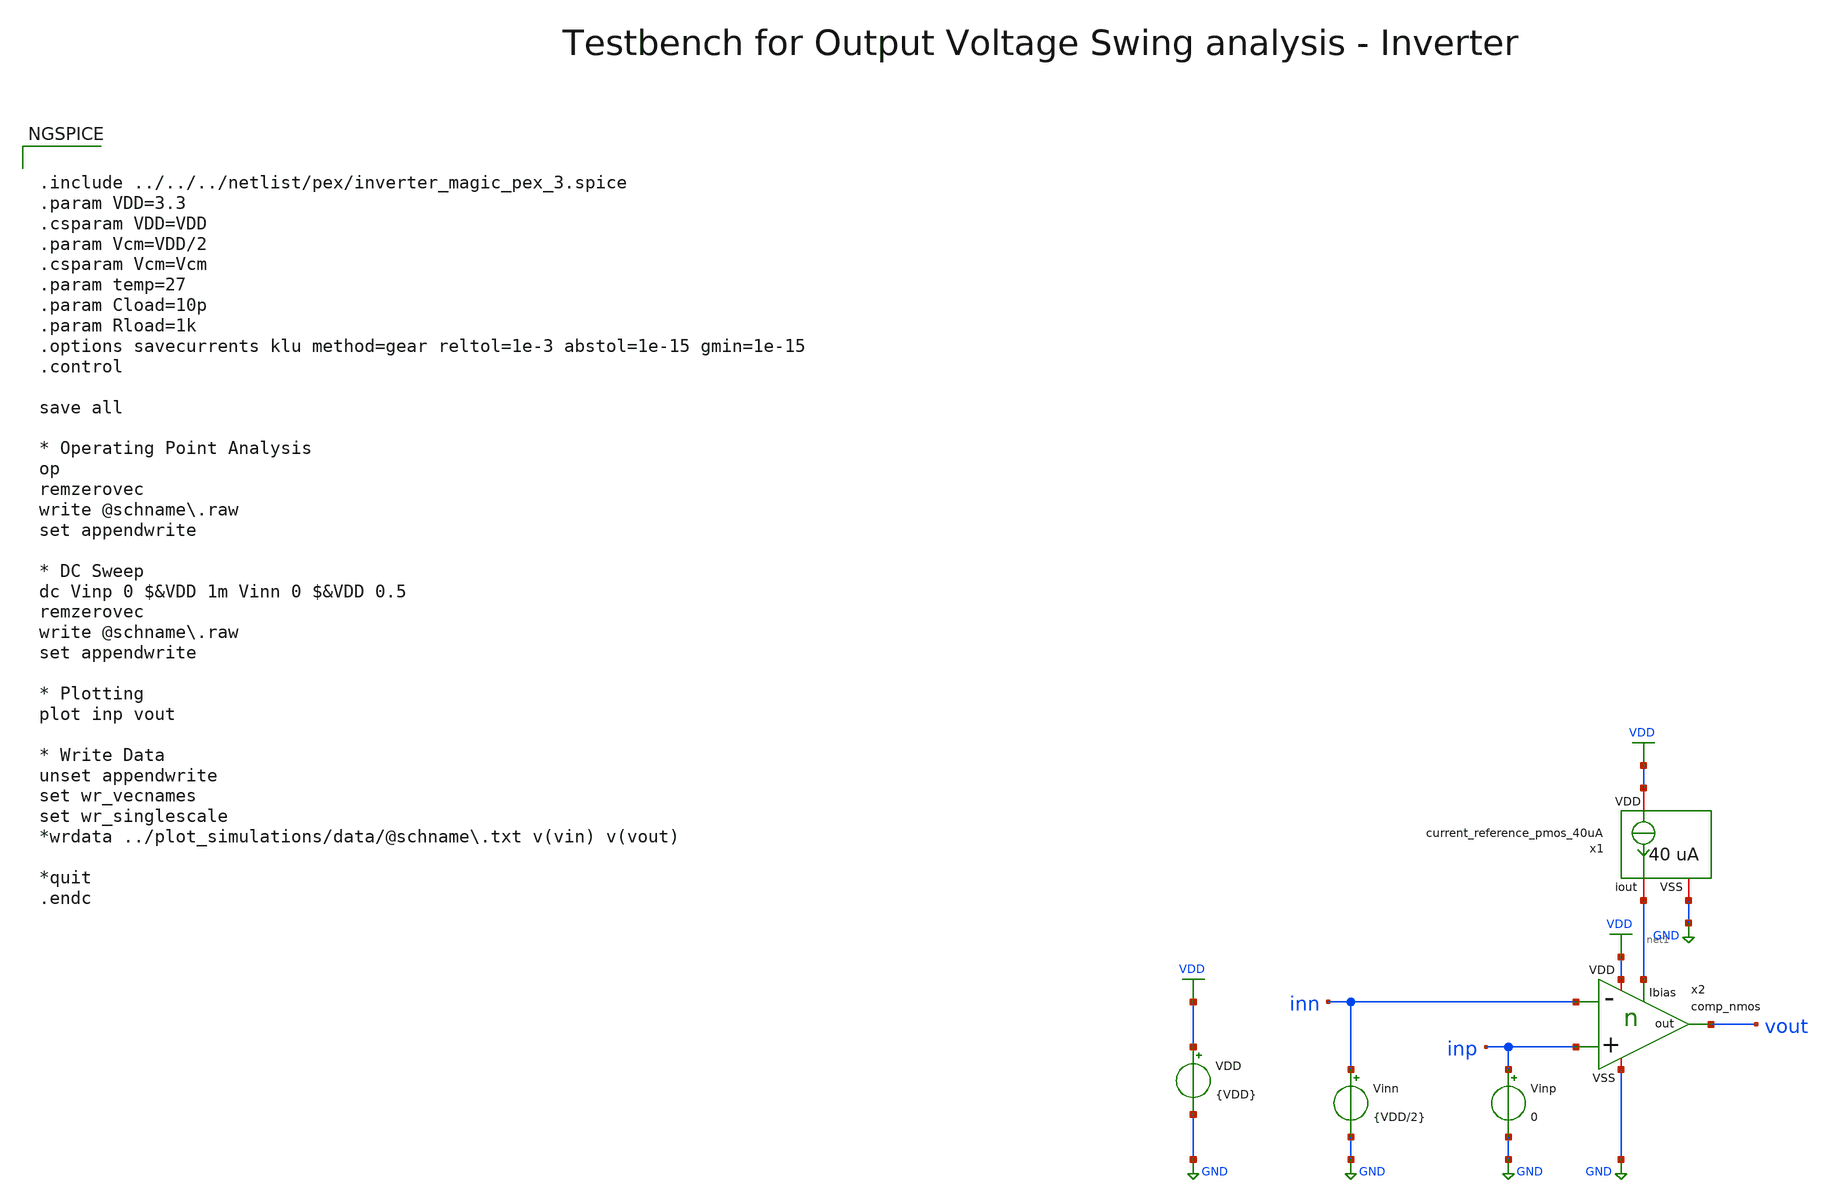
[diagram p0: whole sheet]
** sch_path: macros/heichips26_vcr/macros/switched_capacitor/testbenches/xschem/tb_comp_nmos_dc.sch
**.subckt tb_comp_nmos_dc
VDD VDD GND {VDD}
Vinp inp GND 0
Vinn inn GND {VDD/2}
x1 VDD net1 GND current_reference_pmos_40uA
x2 vout inn inp VDD net1 GND comp_nmos
**** begin user architecture code


.include ../../../netlist/pex/inverter_magic_pex_3.spice
.param VDD=3.3
.csparam VDD=VDD
.param Vcm=VDD/2
.csparam Vcm=Vcm
.param temp=27
.param Cload=10p
.param Rload=1k
.options savecurrents klu method=gear reltol=1e-3 abstol=1e-15 gmin=1e-15
.control

save all

* Operating Point Analysis
op
remzerovec
write @schname\.raw
set appendwrite

* DC Sweep
dc Vinp 0 $&VDD 1m Vinn 0 $&VDD 0.5
remzerovec
write @schname\.raw
set appendwrite

* Plotting
plot inp vout

* Write Data
unset appendwrite
set wr_vecnames
set wr_singlescale
*wrdata ../plot_simulations/data/@schname\.txt v(vin) v(vout)

*quit
.endc



.lib cornerMOSlv.lib mos_tt
.lib cornerMOShv.lib mos_tt
.lib cornerRES.lib res_typ
.lib cornerDIO.lib dio_tt

**** end user architecture code
**.ends

* expanding   symbol:  current_reference_pmos_40uA.sym # of pins=3
** sym_path: macros/heichips26_vcr/macros/switched_capacitor/schematic/xschem/current_reference_pmos_40uA.sym
** sch_path: macros/heichips26_vcr/macros/switched_capacitor/schematic/xschem/current_reference_pmos_40uA.sch
.subckt current_reference_pmos_40uA VDD iout VSS
*.iopin VSS
*.iopin VDD
*.iopin iout
XM8 net1 net2 VSS VSS sg13_hv_nmos w=n_w l=n_l ng=1 m=1 mm_ok=1
XM6 net1 net1 VDD VDD sg13_hv_pmos w=p_w l=p_l ng=1 m=1 mm_ok=1
XM1 net2 net1 net3 VDD sg13_hv_pmos w=p_w l=p_l ng=1 m=1 mm_ok=1
XM3 net2 net2 VSS VSS sg13_hv_nmos w=n_w l=n_l ng=1 m=1 mm_ok=1
XR2 VDD net4 VSS rppd w=2e-6 l=21.6e-6 m=1 b=0 mm_ok=1
XR3 net4 net3 VSS rsil w=0.5e-6 l=282e-6 m=1 mm_ok=1
**** begin user architecture code


.param n_w = 6u
.param n_l = 5u
.param p_w = 10u
.param p_l = 2u


**** end user architecture code
XM2 net2 net1 net3 VDD sg13_hv_pmos w=p_w l=p_l ng=1 m=1 mm_ok=1
XM4 net2 net1 net3 VDD sg13_hv_pmos w=p_w l=p_l ng=1 m=1 mm_ok=1
XM5 net2 net1 net3 VDD sg13_hv_pmos w=p_w l=p_l ng=1 m=1 mm_ok=1
XM7 iout net1 VDD VDD sg13_hv_pmos w=p_w l=p_l ng=1 m=1 mm_ok=1
.ends


* expanding   symbol:  comp_nmos.sym # of pins=6
** sym_path: macros/heichips26_vcr/macros/switched_capacitor/schematic/xschem/comp_nmos.sym
** sch_path: macros/heichips26_vcr/macros/switched_capacitor/schematic/xschem/comp_nmos.sch
.subckt comp_nmos out - + VDD Ibias VSS
*.iopin VDD
*.iopin VSS
*.ipin -
*.ipin +
*.ipin Ibias
*.opin out
XM8 net2 + net3 VSS sg13_hv_nmos w=n_w l=n_l ng=1 m=1 mm_ok=1
XM6 net1 net1 VDD VDD sg13_hv_pmos w=p_w l=p_l ng=1 m=1 mm_ok=1
XM1 net2 net1 VDD VDD sg13_hv_pmos w=p_w l=p_l ng=1 m=1 mm_ok=1
XM3 net1 - net3 VSS sg13_hv_nmos w=n_w l=n_l ng=1 m=1 mm_ok=1
**** begin user architecture code


.param n_w = 1.2u
.param n_l = 1.5u
.param p_w = 2u
.param p_l = 0.4u


**** end user architecture code
XM2 out net2 VDD VDD sg13_hv_pmos w=p_w l=p_l ng=1 m=1 mm_ok=1
XM4 net3 Ibias VSS VSS sg13_hv_nmos w=2*n_w l=n_l ng=1 m=1 mm_ok=1
XM5 out Ibias VSS VSS sg13_hv_nmos w=2*n_w l=n_l ng=1 m=1 mm_ok=1
XM7 Ibias Ibias VSS VSS sg13_hv_nmos w=n_w l=n_l ng=1 m=1 mm_ok=1
.ends

.GLOBAL GND
.GLOBAL VDD
.end
